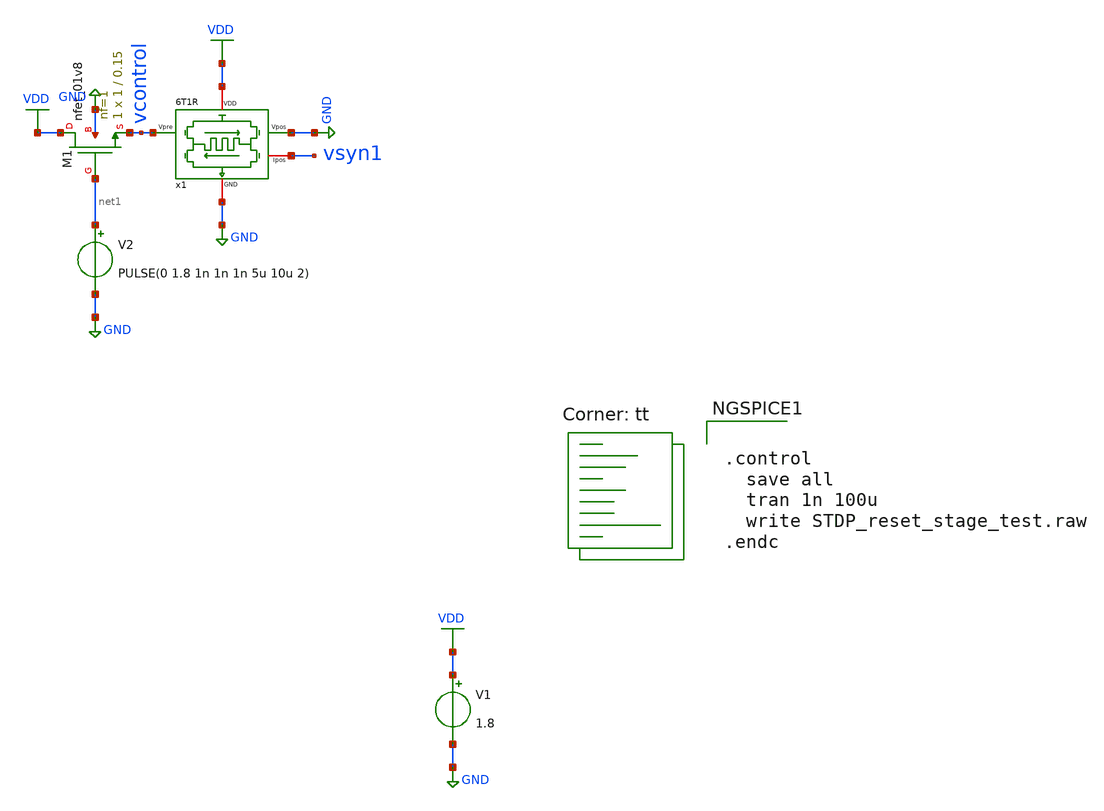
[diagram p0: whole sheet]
** sch_path: STDP/STDP_reset_stage_test.sch
**.subckt STDP_reset_stage_test
V1 VDD GND 1.8
x1 VDD vsyn1 vcontrol GND GND 6T1R
V2 net1 GND PULSE(0 1.8 1n 1n 1n 5u 10u 2)
XM1 VDD net1 vcontrol GND sky130_fd_pr__nfet_01v8 L=0.15 W=1 nf=1 ad='int((nf+1)/2) * W/nf * 0.29' as='int((nf+2)/2) * W/nf * 0.29'
+ pd='2*int((nf+1)/2) * (W/nf + 0.29)' ps='2*int((nf+2)/2) * (W/nf + 0.29)' nrd='0.29 / W' nrs='0.29 / W'
+ sa=0 sb=0 sd=0 mult=1 m=1
**** begin user architecture code
.lib $::SKYWATER_MODELS/sky130.lib.spice tt

** opencircuitdesign pdks install
.inc $::SKYWATER_MODELS/rram_v0.spice



.control
  save all
  tran 1n 100u
  write STDP_reset_stage_test.raw
.endc


**** end user architecture code
**.ends

* expanding   symbol:  /home/ricardo/RATT_repos/Proyectos_xschem/synapse/6T1R.sym # of pins=5
** sym_path: synapse/6T1R.sym
** sch_path: synapse/6T1R.sch
.subckt 6T1R VDD Ipos Vpre Vpos GND
*.ipin Vpre
*.ipin Vpos
*.iopin GND
*.iopin Ipos
*.iopin VDD
XM1 vipre Vpre net1 GND sky130_fd_pr__nfet_01v8 L=0.15 W=10 nf=1 ad='int((nf+1)/2) * W/nf * 0.29' as='int((nf+2)/2) * W/nf * 0.29'
+ pd='2*int((nf+1)/2) * (W/nf + 0.29)' ps='2*int((nf+2)/2) * (W/nf + 0.29)' nrd='0.29 / W' nrs='0.29 / W'
+ sa=0 sb=0 sd=0 mult=1 m=1
XR1 net2 net1 rram_v0
XM3 vipre Vpos net2 GND sky130_fd_pr__nfet_01v8 L=0.15 W=1 nf=1 ad='int((nf+1)/2) * W/nf * 0.29' as='int((nf+2)/2) * W/nf * 0.29'
+ pd='2*int((nf+1)/2) * (W/nf + 0.29)' ps='2*int((nf+2)/2) * (W/nf + 0.29)' nrd='0.29 / W' nrs='0.29 / W'
+ sa=0 sb=0 sd=0 mult=1 m=1
XM6 Ipos vipre VDD VDD sky130_fd_pr__pfet_01v8 L=0.15 W=1 nf=1 ad='int((nf+1)/2) * W/nf * 0.29' as='int((nf+2)/2) * W/nf * 0.29'
+ pd='2*int((nf+1)/2) * (W/nf + 0.29)' ps='2*int((nf+2)/2) * (W/nf + 0.29)' nrd='0.29 / W' nrs='0.29 / W'
+ sa=0 sb=0 sd=0 mult=1 m=1
XM5 vipre vipre VDD VDD sky130_fd_pr__pfet_01v8 L=0.15 W=20 nf=1 ad='int((nf+1)/2) * W/nf * 0.29' as='int((nf+2)/2) * W/nf * 0.29'
+ pd='2*int((nf+1)/2) * (W/nf + 0.29)' ps='2*int((nf+2)/2) * (W/nf + 0.29)' nrd='0.29 / W' nrs='0.29 / W'
+ sa=0 sb=0 sd=0 mult=1 m=1
XM2 net1 Vpos GND GND sky130_fd_pr__nfet_01v8 L=0.15 W=1 nf=1 ad='int((nf+1)/2) * W/nf * 0.29' as='int((nf+2)/2) * W/nf * 0.29'
+ pd='2*int((nf+1)/2) * (W/nf + 0.29)' ps='2*int((nf+2)/2) * (W/nf + 0.29)' nrd='0.29 / W' nrs='0.29 / W'
+ sa=0 sb=0 sd=0 mult=1 m=1
XM4 net2 Vpre GND GND sky130_fd_pr__nfet_01v8 L=0.15 W=10 nf=1 ad='int((nf+1)/2) * W/nf * 0.29' as='int((nf+2)/2) * W/nf * 0.29'
+ pd='2*int((nf+1)/2) * (W/nf + 0.29)' ps='2*int((nf+2)/2) * (W/nf + 0.29)' nrd='0.29 / W' nrs='0.29 / W'
+ sa=0 sb=0 sd=0 mult=1 m=1
.ends

.GLOBAL GND
.GLOBAL VDD
.end
